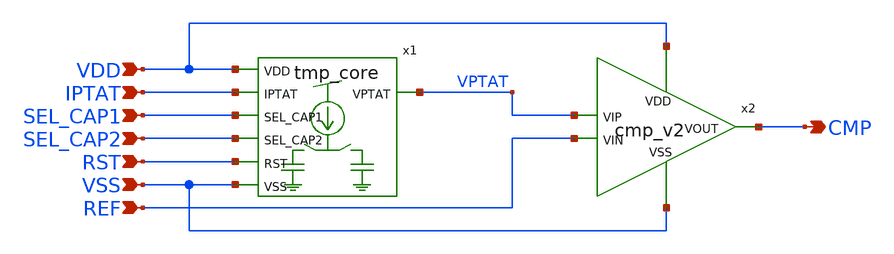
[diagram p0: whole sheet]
** sch_path: design/LELO_TORD_SKY130A/TB_tmp_core_and_cmp.sch
**.subckt TB_tmp_core_and_cmp REF CMP VSS VDD IPTAT RST SEL_CAP1 SEL_CAP2
*.ipin REF
*.opin CMP
*.ipin VSS
*.ipin VDD
*.ipin IPTAT
*.ipin RST
*.ipin SEL_CAP1
*.ipin SEL_CAP2
x2 VDD VPTAT REF CMP VSS cmp_v2
x1 VDD IPTAT SEL_CAP1 SEL_CAP2 VPTAT RST VSS tmp_core
**.ends
.end
